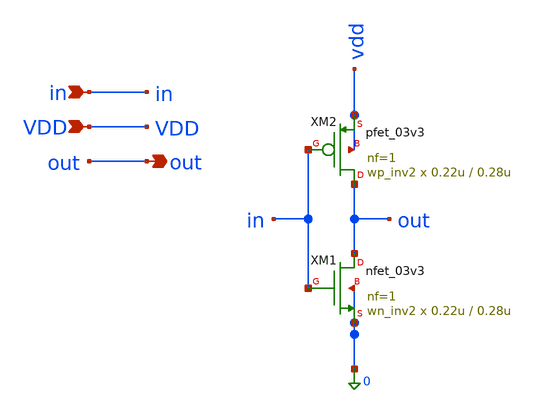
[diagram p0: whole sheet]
** sch_path: Design_Files/IC Design/Schematic/SAR_ADC_BLOCKS/INV2/INV2.sch
**.subckt INV2 in VDD out
*.ipin in
*.ipin VDD
*.opin out
XM1 out in 0 0 nfet_03v3 L=0.28u W=0.22u nf=1 ad='int((nf+1)/2) * W/nf * 0.18u' as='int((nf+2)/2) * W/nf * 0.18u'
+ pd='2*int((nf+1)/2) * (W/nf + 0.18u)' ps='2*int((nf+2)/2) * (W/nf + 0.18u)' nrd='0.18u / W' nrs='0.18u / W'
+ sa=0 sb=0 sd=0 m=wn_inv2
XM2 out in vdd vdd pfet_03v3 L=0.28u W=0.22u nf=1 ad='int((nf+1)/2) * W/nf * 0.18u' as='int((nf+2)/2) * W/nf * 0.18u'
+ pd='2*int((nf+1)/2) * (W/nf + 0.18u)' ps='2*int((nf+2)/2) * (W/nf + 0.18u)' nrd='0.18u / W' nrs='0.18u / W'
+ sa=0 sb=0 sd=0 m=wp_inv2
**.ends
.end
